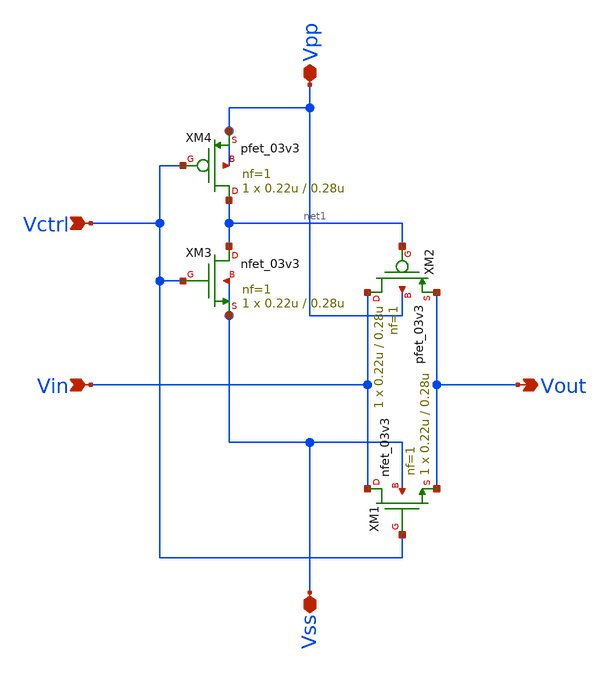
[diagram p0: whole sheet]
** sch_path: blocks/analog-mux/Tgate-activeHigh-LI.sch
**.subckt Tgate-activeHigh-LI Vin Vout Vctrl Vpp Vss
*.ipin Vin
*.opin Vout
*.ipin Vctrl
*.iopin Vpp
*.iopin Vss
XM1 Vin Vctrl Vout Vss nfet_03v3 L=0.28u W=0.22u nf=1 ad='int((nf+1)/2) * W/nf * 0.18u' as='int((nf+2)/2) * W/nf * 0.18u'
+ pd='2*int((nf+1)/2) * (W/nf + 0.18u)' ps='2*int((nf+2)/2) * (W/nf + 0.18u)' nrd='0.18u / W' nrs='0.18u / W'
+ sa=0 sb=0 sd=0 m=1
XM2 Vin net1 Vout Vpp pfet_03v3 L=0.28u W=0.22u nf=1 ad='int((nf+1)/2) * W/nf * 0.18u' as='int((nf+2)/2) * W/nf * 0.18u'
+ pd='2*int((nf+1)/2) * (W/nf + 0.18u)' ps='2*int((nf+2)/2) * (W/nf + 0.18u)' nrd='0.18u / W' nrs='0.18u / W'
+ sa=0 sb=0 sd=0 m=1
XM3 net1 Vctrl Vss Vss nfet_03v3 L=0.28u W=0.22u nf=1 ad='int((nf+1)/2) * W/nf * 0.18u' as='int((nf+2)/2) * W/nf * 0.18u'
+ pd='2*int((nf+1)/2) * (W/nf + 0.18u)' ps='2*int((nf+2)/2) * (W/nf + 0.18u)' nrd='0.18u / W' nrs='0.18u / W'
+ sa=0 sb=0 sd=0 m=1
XM4 net1 Vctrl Vpp Vpp pfet_03v3 L=0.28u W=0.22u nf=1 ad='int((nf+1)/2) * W/nf * 0.18u' as='int((nf+2)/2) * W/nf * 0.18u'
+ pd='2*int((nf+1)/2) * (W/nf + 0.18u)' ps='2*int((nf+2)/2) * (W/nf + 0.18u)' nrd='0.18u / W' nrs='0.18u / W'
+ sa=0 sb=0 sd=0 m=1
**.ends
.end
